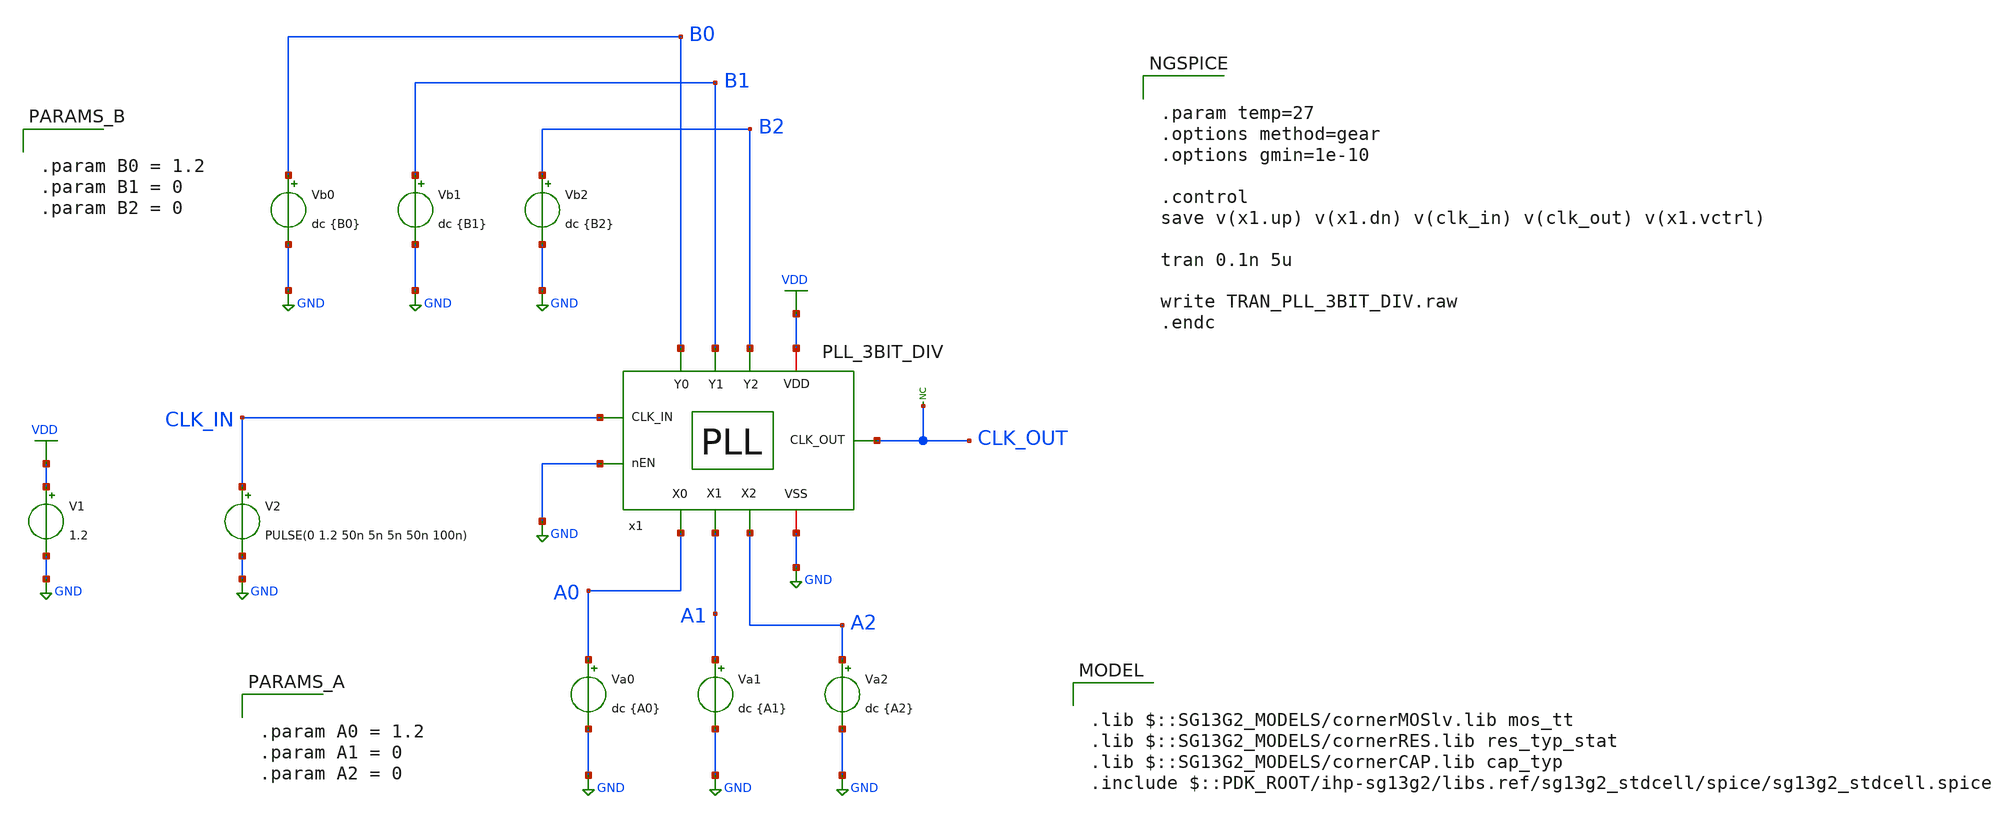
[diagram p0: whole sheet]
** sch_path: 30_MHz_Fractional_N_PLL/design_data/xschem/PLL_3BIT_DIV_TB.sch
* IHP-GmbH/IHP-Open-PDK/ihp-sg13g2/libs.tech/xschem/sg13g2_stdcells/sg13g2_or3_1.sch:
* Copyright 2023 IHP PDK Authors
* Licensed under the Apache License, Version 2.0 (the "License");

.lib $::SG13G2_MODELS/cornerMOSlv.lib mos_tt
.lib $::SG13G2_MODELS/cornerRES.lib res_typ_stat
.lib $::SG13G2_MODELS/cornerCAP.lib cap_typ
.include $::PDK_ROOT/ihp-sg13g2/libs.ref/sg13g2_stdcell/spice/sg13g2_stdcell.spice

**.subckt PLL_3BIT_DIV_TB
V1 VDD GND 1.2
V2 CLK_IN GND PULSE(0 1.2 50n 5n 5n 50n 100n)
Va0 A0 GND dc {A0}
Va1 A1 GND dc {A1}
* noconn CLK_OUT
Va2 A2 GND dc {A2}
Vb0 B0 GND dc {B0}
Vb1 B1 GND dc {B1}
Vb2 B2 GND dc {B2}
x1 CLK_IN CLK_OUT B0 B2 B1 VDD GND GND A1 A2 A0 PLL_3BIT_DIV
**** begin user architecture code


.param temp=27
.options method=gear
.options gmin=1e-10

.control
save v(x1.up) v(x1.dn) v(clk_in) v(clk_out) v(x1.vctrl)

tran 0.1n 5u

write TRAN_PLL_3BIT_DIV.raw
.endc





.param A0 = 1.2
.param A1 = 0
.param A2 = 0




.param B0 = 1.2
.param B1 = 0
.param B2 = 0




.ic V(VDD) = 1.2
.ic V(x1.up) = 0
.ic V(x1.dn) = 0
.ic V(x1.vctrl) = 0.7


**** end user architecture code
**.ends

* expanding   symbol:  PLL_3BIT_DIV.sym # of pins=11
** sym_path: 30_MHz_Fractional_N_PLL/design_data/xschem/PLL_3BIT_DIV.sym
** sch_path: 30_MHz_Fractional_N_PLL/design_data/xschem/PLL_3BIT_DIV.sch
.subckt PLL_3BIT_DIV CLK_IN CLK_OUT Y0 Y2 Y1 VDD VSS nEN X1 X2 X0
*.iopin VSS
*.iopin VDD
*.ipin CLK_IN
*.opin CLK_OUT
*.ipin X0
*.ipin X1
*.ipin nEN
*.ipin X2
*.ipin Y0
*.ipin Y1
*.ipin Y2
x3 VDD VDD VSS VSS EN BIAS_N BIAS_P nEN BIAS_GEN
x5 VDD UP VSS DN CLK_IN DIV_OUT PFD
x2 VDD BIAS_P UP VOUT_CP DN BIAS_N VSS CHRG_PUMP
x1 VOUT_CP VCTRL VSS LOOP_FILTER
x6 EN nEN VDD VSS sg13g2_inv_1
x7 X0 VCO_OUT EN DIV_OUT X1 VDD VSS X2 3BIT_FREQ_DIV
x9 Y0 VCO_OUT EN CLK_OUT Y1 VDD VSS Y2 3BIT_FREQ_DIV
x4 VDD VSS VCTRL VCO_OUT 11STG_VCO
.ends


* expanding   symbol:  BIAS_GEN.sym # of pins=8
** sym_path: 30_MHz_Fractional_N_PLL/design_data/xschem/BIAS_GEN.sym
** sch_path: 30_MHz_Fractional_N_PLL/design_data/xschem/BIAS_GEN.sch
.subckt BIAS_GEN VPWR VPB VGND VNB en bias_n bias_p enb
*.ipin en
*.opin bias_n
*.iopin VNB
*.iopin VGND
*.iopin VPB
*.iopin VPWR
*.ipin enb
*.opin bias_p
XM1 bias_p kick kick_sw VNB sg13_lv_nmos w=0.5u l=0.15u ng=1 m=1 mm_ok=1
XM2 kick_sw en VGND VNB sg13_lv_nmos w=0.5u l=0.15u ng=1 m=1 mm_ok=1
XM3 kick bias_n VGND VNB sg13_lv_nmos w=1.0u l=1.0u ng=1 m=1 mm_ok=1
XM4 bias_p bias_n net1 VNB sg13_lv_nmos w=1.0u l=1.0u ng=1 m=1 mm_ok=1
XM5 bias_n enb VGND VNB sg13_lv_nmos w=0.5u l=0.15u ng=1 m=1 mm_ok=1
XM6 bias_n bias_n VGND VNB sg13_lv_nmos w=1.0u l=1.0u ng=1 m=1 mm_ok=1
XM7 kick kick dio_mid VPB sg13_lv_pmos w=0.5u l=0.15u ng=1 m=1 mm_ok=1
XM8 bias_p bias_p VPWR VPB sg13_lv_pmos w=2.0u l=1.0u ng=1 m=1 mm_ok=1
XM9 bias_p en VPWR VPB sg13_lv_pmos w=0.5u l=0.15u ng=1 m=1 mm_ok=1
XM10 bias_n bias_p res_bot VPB sg13_lv_pmos w=4.0u l=1.0u ng=1 m=1 mm_ok=1
XM11 kick en VPWR VPB sg13_lv_pmos w=0.5u l=0.15u ng=1 m=1 mm_ok=1
XM12 dio_mid dio_mid VPWR VPB sg13_lv_pmos w=0.5u l=0.15u ng=1 m=1 mm_ok=1
XR1 VPWR res_bot sub! rhigh w=1.0e-6 l=12.0e-6 m=1 b=0 mm_ok=1
XR2 net1 VGND sub! rhigh w=1.0e-6 l=12.0e-6 m=1 b=0 mm_ok=1
.ends


* expanding   symbol:  PFD.sym # of pins=6
** sym_path: 30_MHz_Fractional_N_PLL/design_data/xschem/PFD.sym
** sch_path: 30_MHz_Fractional_N_PLL/design_data/xschem/PFD.sch
.subckt PFD vdd up vss down ref_clk vco_clk
*.iopin vdd
*.ipin ref_clk
*.iopin vss
*.ipin vco_clk
*.opin up
*.opin down
XM1 net2 vco_clk vss vss sg13_lv_nmos w=0.36u l=0.15u ng=1 m=1 mm_ok=1
XM4 net1 ref_clk net2 vss sg13_lv_nmos w=1.8u l=0.15u ng=1 m=1 mm_ok=1
XM5 net3 ref_clk net1 vss sg13_lv_nmos w=0.84u l=0.15u ng=1 m=1 mm_ok=1
XM9 net3 ref_clk ref_clk vdd sg13_lv_pmos w=0.64u l=0.15u ng=1 m=1 mm_ok=1
XM11 net7 net3 vss vss sg13_lv_nmos w=0.36u l=0.15u ng=1 m=1 mm_ok=1
XM12 vdd net3 net7 vdd sg13_lv_pmos w=0.72u l=0.15u ng=1 m=1 mm_ok=1
XM13 up net7 vss vss sg13_lv_nmos w=0.48u l=0.15u ng=1 m=1 mm_ok=1
XM14 vdd net7 up vdd sg13_lv_pmos w=0.96u l=0.15u ng=1 m=1 mm_ok=1
XM3 net1 ref_clk vdd vdd sg13_lv_pmos w=0.64u l=0.15u ng=1 m=1 mm_ok=1
XM6 net4 vco_clk vdd vdd sg13_lv_pmos w=0.64u l=0.15u ng=1 m=1 mm_ok=1
XM7 net4 vco_clk net5 vss sg13_lv_nmos w=1.8u l=0.15u ng=1 m=1 mm_ok=1
XM19 net5 ref_clk vss vss sg13_lv_nmos w=0.36u l=0.15u ng=1 m=1 mm_ok=1
XM8 net6 vco_clk net4 vss sg13_lv_nmos w=0.84u l=0.15u ng=1 m=1 mm_ok=1
XM10 net6 vco_clk vco_clk vdd sg13_lv_pmos w=0.64u l=0.15u ng=1 m=1 mm_ok=1
XM15 vdd net6 net8 vdd sg13_lv_pmos w=0.72u l=0.15u ng=1 m=1 mm_ok=1
XM16 net8 net6 vss vss sg13_lv_nmos w=0.36u l=0.15u ng=1 m=1 mm_ok=1
XM17 vdd net8 down vdd sg13_lv_pmos w=0.96u l=0.15u ng=1 m=1 mm_ok=1
XM18 down net8 vss vss sg13_lv_nmos w=0.48u l=0.15u ng=1 m=1 mm_ok=1
.ends


* expanding   symbol:  CHRG_PUMP.sym # of pins=7
** sym_path: 30_MHz_Fractional_N_PLL/design_data/xschem/CHRG_PUMP.sym
** sch_path: 30_MHz_Fractional_N_PLL/design_data/xschem/CHRG_PUMP.sch
.subckt CHRG_PUMP VP bias_p up vout down bias_n VN
*.ipin bias_p
*.ipin up
*.ipin down
*.ipin bias_n
*.iopin VN
*.iopin VP
*.opin vout
XM1 net1 bias_n VN VN sg13_lv_nmos w=1.2u l=0.13u ng=1 m=1 mm_ok=1
XM2 vout down net1 VN sg13_lv_nmos w=1.2u l=0.13u ng=1 m=1 mm_ok=1
XM3 vout net3 net2 VP sg13_lv_pmos w=0.15u l=0.13u ng=1 m=1 mm_ok=1
XM4 net2 bias_p VP VP sg13_lv_pmos w=0.15u l=0.13u ng=1 m=1 mm_ok=1
x1 VP up net3 VN INV
.ends


* expanding   symbol:  LOOP_FILTER.sym # of pins=3
** sym_path: 30_MHz_Fractional_N_PLL/design_data/xschem/LOOP_FILTER.sym
** sch_path: 30_MHz_Fractional_N_PLL/design_data/xschem/LOOP_FILTER.sch
.subckt LOOP_FILTER vin vout VN
*.iopin VN
*.ipin vin
*.opin vout
XR1 vout vin sub! rhigh w=0.6e-6 l=0.96e-6 m=1 b=0 mm_ok=1
XM1 VN net1 VN VN sg13_lv_nmos w=0.5u l=0.650u ng=1 m=15 mm_ok=1
XM2 VN vout VN VN sg13_lv_nmos w=0.15u l=0.13u ng=1 m=1 mm_ok=1
XM3 VN net1 VN VN sg13_lv_nmos w=0.5u l=0.650u ng=1 m=15 mm_ok=1
XM4 VN vout VN VN sg13_lv_nmos w=0.15u l=0.13u ng=1 m=1 mm_ok=1
XR2 net1 vin sub! rhigh w=0.5e-6 l=0.96e-6 m=1 b=0 mm_ok=1
XM5 VN vin VN VN sg13_lv_nmos w=1.5u l=0.650u ng=1 m=15 mm_ok=1
XM6 VN vin VN VN sg13_lv_nmos w=1.5u l=0.650u ng=1 m=15 mm_ok=1
.ends


* expanding   symbol:  sg13g2_stdcells/sg13g2_inv_1.sym # of pins=2
** sym_path: sg13g2_stdcells/sg13g2_inv_1.sym
** sch_path: sg13g2_stdcells/sg13g2_inv_1.sch
.subckt sg13g2_inv_1 Y A VDD VSS
*.opin Y
*.ipin A
*.iopin VDD
*.iopin VSS
XM1 Y A VSS VSS sg13_lv_nmos w=740.00n l=130.00n ng=1 m=1 mm_ok=1
XM2 Y A VDD VDD sg13_lv_pmos w=1.12u l=130.00n ng=1 m=1 mm_ok=1
.ends


* expanding   symbol:  3BIT_FREQ_DIV.sym # of pins=8
** sym_path: 30_MHz_Fractional_N_PLL/design_data/xschem/3BIT_FREQ_DIV.sym
** sch_path: 30_MHz_Fractional_N_PLL/design_data/xschem/3BIT_FREQ_DIV.sch
.subckt 3BIT_FREQ_DIV A0 CLK_IN EN CLK_OUT A1 VDD VSS A2
*.ipin CLK_IN
*.ipin EN
*.ipin A0
*.ipin A1
*.opin CLK_OUT
*.iopin VSS
*.iopin VDD
*.ipin A2
x1 VDD VSS nEQ0 net1 CLK net2 DIV_RST A0 FREQ_DIV_CELL
x2 VDD VSS nEQ1 net2 CLK net5 DIV_RST A1 FREQ_DIV_CELL
x3 net6 VDD VSS sg13g2_tiehi
x5 DIV_RST CLK_OUT net3 net3 net4 VDD VSS DFF_nCLK
x6 net7 VDD VSS sg13g2_tiehi
* noconn CLK_OUT
x7 CLK CLK_IN EN VDD VSS sg13g2_nand2_1
x4 DIV_RST nEQ2 nEQ1 nEQ0 VDD VSS sg13g2_or3_1
x8 VDD VSS nEQ2 net5 CLK Cout DIV_RST A2 FREQ_DIV_CELL
* noconn Cout
.ends


* expanding   symbol:  11STG_VCO.sym # of pins=4
** sym_path: 30_MHz_Fractional_N_PLL/design_data/xschem/11STG_VCO.sym
** sch_path: 30_MHz_Fractional_N_PLL/design_data/xschem/11STG_VCO.sch
.subckt 11STG_VCO VPWR VGND vctl Vout
*.iopin VPWR
*.iopin VGND
*.ipin vctl
*.opin Vout
XM21 mirror_pg mirror_pg VPWR VPWR sg13_lv_pmos w=0.8u l=0.13u ng=1 m=1 mm_ok=1
XM22 net1 mirror_pg VPWR VPWR sg13_lv_pmos w=0.8u l=0.13u ng=1 m=1 mm_ok=1
XM23 net2 mirror_pg VPWR VPWR sg13_lv_pmos w=0.8u l=0.13u ng=1 m=1 mm_ok=1
XM24 net3 mirror_pg VPWR VPWR sg13_lv_pmos w=0.8u l=0.13u ng=1 m=1 mm_ok=1
XM25 mirror_pg vctl VGND VGND sg13_lv_nmos w=0.6u l=0.13u ng=1 m=1 mm_ok=1
XM26 net9 vctl VGND VGND sg13_lv_nmos w=0.6u l=0.13u ng=1 m=1 mm_ok=1
XM28 net7 vctl VGND VGND sg13_lv_nmos w=0.6u l=0.13u ng=1 m=1 mm_ok=1
XM29 net13 mirror_pg VPWR VPWR sg13_lv_pmos w=0.8u l=0.13u ng=1 m=1 mm_ok=1
XM30 net12 mirror_pg VPWR VPWR sg13_lv_pmos w=0.8u l=0.13u ng=1 m=1 mm_ok=1
XM31 net10 vctl VGND VGND sg13_lv_nmos w=0.6u l=0.13u ng=1 m=1 mm_ok=1
XM32 net11 vctl VGND VGND sg13_lv_nmos w=0.6u l=0.13u ng=1 m=1 mm_ok=1
XM33 net15 mirror_pg VPWR VPWR sg13_lv_pmos w=0.8u l=0.13u ng=1 m=1 mm_ok=1
XM34 net16 mirror_pg VPWR VPWR sg13_lv_pmos w=0.8u l=0.13u ng=1 m=1 mm_ok=1
XM35 net20 vctl VGND VGND sg13_lv_nmos w=0.6u l=0.13u ng=1 m=1 mm_ok=1
XM36 net19 vctl VGND VGND sg13_lv_nmos w=0.6u l=0.13u ng=1 m=1 mm_ok=1
XM37 net24 mirror_pg VPWR VPWR sg13_lv_pmos w=0.8u l=0.13u ng=1 m=1 mm_ok=1
XM38 net23 mirror_pg VPWR VPWR sg13_lv_pmos w=0.8u l=0.13u ng=1 m=1 mm_ok=1
XM39 net21 vctl VGND VGND sg13_lv_nmos w=0.6u l=0.13u ng=1 m=1 mm_ok=1
XM40 net22 vctl VGND VGND sg13_lv_nmos w=0.6u l=0.13u ng=1 m=1 mm_ok=1
XM41 net31 mirror_pg VPWR VPWR sg13_lv_pmos w=0.8u l=0.13u ng=1 m=1 mm_ok=1
XM42 net30 mirror_pg VPWR VPWR sg13_lv_pmos w=0.8u l=0.13u ng=1 m=1 mm_ok=1
XM43 net28 vctl VGND VGND sg13_lv_nmos w=0.6u l=0.13u ng=1 m=1 mm_ok=1
XM44 net29 vctl VGND VGND sg13_lv_nmos w=0.6u l=0.13u ng=1 m=1 mm_ok=1
XM1 net8 vctl VGND VGND sg13_lv_nmos w=0.6u l=0.13u ng=1 m=1 mm_ok=1
XC12 net4 VGND cap_cmim w=6.99e-6 l=6.99e-6 m=1 mm_ok=1
XC1 net5 VGND cap_cmim w=6.99e-6 l=6.99e-6 m=1 mm_ok=1
XC2 net6 VGND cap_cmim w=6.99e-6 l=6.99e-6 m=1 mm_ok=1
XC3 net14 VGND cap_cmim w=6.99e-6 l=6.99e-6 m=1 mm_ok=1
XC4 net26 VGND cap_cmim w=6.99e-6 l=6.99e-6 m=1 mm_ok=1
XC5 net17 VGND cap_cmim w=6.99e-6 l=6.99e-6 m=1 mm_ok=1
XC6 net18 VGND cap_cmim w=6.99e-6 l=6.99e-6 m=1 mm_ok=1
XC7 net25 VGND cap_cmim w=6.99e-6 l=6.99e-6 m=1 mm_ok=1
XC8 net27 VGND cap_cmim w=6.99e-6 l=6.99e-6 m=1 mm_ok=1
XC9 net32 VGND cap_cmim w=6.99e-6 l=6.99e-6 m=1 mm_ok=1
XC10 Vout VGND cap_cmim w=6.99e-6 l=6.99e-6 m=1 mm_ok=1
x1 net1 VPWR Vout net4 VGND net9 VCO_INV
x2 net2 VPWR net4 net5 VGND net8 VCO_INV
x3 net3 VPWR net5 net6 VGND net7 VCO_INV
x4 net13 VPWR net6 net14 VGND net10 VCO_INV
x5 net12 VPWR net14 net26 VGND net11 VCO_INV
x6 net15 VPWR net26 net17 VGND net20 VCO_INV
x7 net16 VPWR net17 net18 VGND net19 VCO_INV
x8 net24 VPWR net18 net25 VGND net21 VCO_INV
x9 net23 VPWR net25 net27 VGND net22 VCO_INV
x10 net31 VPWR net27 net32 VGND net28 VCO_INV
x11 net30 VPWR net32 Vout VGND net29 VCO_INV
.ends


* expanding   symbol:  INV.sym # of pins=4
** sym_path: 30_MHz_Fractional_N_PLL/design_data/xschem/INV.sym
** sch_path: 30_MHz_Fractional_N_PLL/design_data/xschem/INV.sch
.subckt INV VP IN OUT VN
*.iopin VN
*.iopin VP
*.ipin IN
*.opin OUT
XM1 OUT IN VN VN sg13_lv_nmos w=0.15u l=0.13u ng=1 m=1 mm_ok=1
XM2 OUT IN VP VP sg13_lv_pmos w=0.3u l=0.13u ng=1 m=1 mm_ok=1
.ends


* expanding   symbol:  FREQ_DIV_CELL.sym # of pins=8
** sym_path: 30_MHz_Fractional_N_PLL/design_data/xschem/FREQ_DIV_CELL.sym
** sch_path: 30_MHz_Fractional_N_PLL/design_data/xschem/FREQ_DIV_CELL.sch
.subckt FREQ_DIV_CELL VDD VSS DIV Cin CLK Cout nRST BIT
*.ipin Cin
*.ipin CLK
*.ipin nRST
*.ipin BIT
*.opin DIV
*.opin Cout
*.iopin VSS
*.iopin VDD
x2 CLK net2 net1 net3 nRST VDD VSS DFF_nCLK
x3 DIV net2 BIT VDD VSS sg13g2_xor2_1
* noconn #net3
x1 net2 net1 Cin VDD VSS Cout HALF_ADD
.ends


* expanding   symbol:  DFF_nCLK.sym # of pins=7
** sym_path: 30_MHz_Fractional_N_PLL/design_data/xschem/DFF_nCLK.sym
** sch_path: 30_MHz_Fractional_N_PLL/design_data/xschem/DFF_nCLK.sch
.subckt DFF_nCLK nCLK Q D nQ nRST VDD VSS
*.ipin nCLK
*.ipin D
*.ipin nRST
*.opin Q
*.opin nQ
*.iopin VSS
*.iopin VDD
x1 Q nQ net1 D nRST VDD VSS sg13g2_dfrbp_1
x2 net1 nCLK VDD VSS sg13g2_inv_1
.ends


* expanding   symbol:  sg13g2_stdcells/sg13g2_nand2_1.sym # of pins=3
** sym_path: sg13g2_stdcells/sg13g2_nand2_1.sym
** sch_path: sg13g2_stdcells/sg13g2_nand2_1.sch
.subckt sg13g2_nand2_1 Y A B VDD VSS
*.iopin VDD
*.iopin VSS
*.ipin A
*.ipin B
*.opin Y
XM1 Y A net1 VSS sg13_lv_nmos w=740.00n l=130.00n ng=1 m=1 mm_ok=1
XM2 net1 B VSS VSS sg13_lv_nmos w=740.00n l=130.00n ng=1 m=1 mm_ok=1
XM3 Y A VDD VDD sg13_lv_pmos w=1.12u l=130.00n ng=1 m=1 mm_ok=1
XM4 Y B VDD VDD sg13_lv_pmos w=1.12u l=130.00n ng=1 m=1 mm_ok=1
.ends


* expanding   symbol:  sg13g2_stdcells/sg13g2_or3_1.sym # of pins=4
** sym_path: sg13g2_stdcells/sg13g2_or3_1.sym
** sch_path: sg13g2_stdcells/sg13g2_or3_1.sch
.subckt sg13g2_or3_1 X A B C VDD VSS
*.opin X
*.ipin C
*.ipin B
*.ipin A
*.iopin VDD
*.iopin VSS
XM1 net2 A VSS VSS sg13_lv_nmos w=550.00n l=130.00n ng=1 m=1 mm_ok=1
XM2 net2 B VSS VSS sg13_lv_nmos w=550.00n l=130.00n ng=1 m=1 mm_ok=1
XM3 net2 C VSS VSS sg13_lv_nmos w=550.00n l=130.00n ng=1 m=1 mm_ok=1
XM4 X net2 VSS VSS sg13_lv_nmos w=740.00n l=130.00n ng=1 m=1 mm_ok=1
XM5 net1 A VDD VDD sg13_lv_pmos w=1.000u l=130.00n ng=1 m=1 mm_ok=1
XM6 net3 B net1 VDD sg13_lv_pmos w=1.000u l=130.00n ng=1 m=1 mm_ok=1
XM7 net2 C net3 VDD sg13_lv_pmos w=1.000u l=130.00n ng=1 m=1 mm_ok=1
XM8 X net2 VDD VDD sg13_lv_pmos w=1.12u l=130.00n ng=1 m=1 mm_ok=1
.ends


* expanding   symbol:  VCO_INV.sym # of pins=6
** sym_path: 30_MHz_Fractional_N_PLL/design_data/xschem/VCO_INV.sym
** sch_path: 30_MHz_Fractional_N_PLL/design_data/xschem/VCO_INV.sch
.subckt VCO_INV VPWR VPB A Y VNB VGND
*.iopin VPWR
*.iopin VGND
*.ipin A
*.opin Y
*.iopin VPB
*.iopin VNB
XM2 Y A VPWR VPB sg13_lv_pmos w=2u l=0.13u ng=1 m=1 mm_ok=1
XM1 Y A VGND VNB sg13_lv_nmos w=1u l=0.13u ng=1 m=1 mm_ok=1
.ends


* expanding   symbol:  sg13g2_stdcells/sg13g2_xor2_1.sym # of pins=3
** sym_path: sg13g2_stdcells/sg13g2_xor2_1.sym
** sch_path: sg13g2_stdcells/sg13g2_xor2_1.sch
.subckt sg13g2_xor2_1 X A B VDD VSS
*.opin X
*.ipin B
*.ipin A
*.iopin VDD
*.iopin VSS
XM1 net1 A VSS VSS sg13_lv_nmos w=550.00n l=130.00n ng=1 m=1 mm_ok=1
XM2 net1 B VSS VSS sg13_lv_nmos w=550.00n l=130.00n ng=1 m=1 mm_ok=1
XM3 X net1 VSS VSS sg13_lv_nmos w=740.00n l=130.00n ng=1 m=1 mm_ok=1
XM4 X B net3 VSS sg13_lv_nmos w=740.00n l=130.00n ng=1 m=1 mm_ok=1
XM5 net3 A VSS VSS sg13_lv_nmos w=740.00n l=130.00n ng=1 m=1 mm_ok=1
XM6 net4 A VDD VDD sg13_lv_pmos w=1.000u l=130.00n ng=1 m=1 mm_ok=1
XM7 net1 B net4 VDD sg13_lv_pmos w=1.000u l=130.00n ng=1 m=1 mm_ok=1
XM8 net2 A VDD VDD sg13_lv_pmos w=1.12u l=130.00n ng=1 m=1 mm_ok=1
XM9 X net1 net2 VDD sg13_lv_pmos w=1.12u l=130.00n ng=1 m=1 mm_ok=1
XM10 net2 B VDD VDD sg13_lv_pmos w=1.12u l=130.00n ng=1 m=1 mm_ok=1
.ends


* expanding   symbol:  HALF_ADD.sym # of pins=6
** sym_path: 30_MHz_Fractional_N_PLL/design_data/xschem/HALF_ADD.sym
** sch_path: 30_MHz_Fractional_N_PLL/design_data/xschem/HALF_ADD.sch
.subckt HALF_ADD inB sum inA VDD VSS cout
*.ipin inA
*.ipin inB
*.opin sum
*.opin cout
*.iopin VSS
*.iopin VDD
x1 sum inA inB VDD VSS sg13g2_xor2_1
x2 cout inA inB VDD VSS sg13g2_and2_1
.ends


* expanding   symbol:  sg13g2_stdcells/sg13g2_dfrbp_1.sym # of pins=5
** sym_path: sg13g2_stdcells/sg13g2_dfrbp_1.sym
** sch_path: sg13g2_stdcells/sg13g2_dfrbp_1.sch
.subckt sg13g2_dfrbp_1 Q Q_N CLK D RESET_B VDD VSS
*.ipin D
*.ipin RESET_B
*.ipin CLK
*.opin Q
*.opin Q_N
*.iopin VDD
*.iopin VSS
XM1 Db D net10 VSS sg13_lv_nmos w=420.00n l=130.00n ng=1 m=1 mm_ok=1
XM2 net10 RESET_B VSS VSS sg13_lv_nmos w=420.00n l=130.00n ng=1 m=1 mm_ok=1
XM3 net1 clkneg net9 VSS sg13_lv_nmos w=420.00n l=130.00n ng=1 m=1 mm_ok=1
XM4 net9 net1 VSS VSS sg13_lv_nmos w=420.00n l=130.00n ng=1 m=1 mm_ok=1
XM5 net1 net1 net5 VSS sg13_lv_nmos w=420.00n l=130.00n ng=1 m=1 mm_ok=1
XM6 net5 RESET_B VSS VSS sg13_lv_nmos w=420.00n l=130.00n ng=1 m=1 mm_ok=1
XM7 Q_N net1 VSS VSS sg13_lv_nmos w=740.00n l=130.00n ng=1 m=1 mm_ok=1
XM8 net2 net1 VSS VSS sg13_lv_nmos w=740.00n l=130.00n ng=1 m=1 mm_ok=1
XM9 Q net2 VSS VSS sg13_lv_nmos w=740.00n l=130.00n ng=1 m=1 mm_ok=1
XM10 clkneg CLK VSS VSS sg13_lv_nmos w=740.00n l=130.00n ng=1 m=1 mm_ok=1
XM11 clkpos clkneg VSS VSS sg13_lv_nmos w=740.00n l=130.00n ng=1 m=1 mm_ok=1
XM12 Db clkneg net3 VSS sg13_lv_nmos w=420.00n l=130.00n ng=1 m=1 mm_ok=1
XM13 net3 clkpos net8 VSS sg13_lv_nmos w=420.00n l=130.00n ng=1 m=1 mm_ok=1
XM14 net8 net3 net4 VSS sg13_lv_nmos w=420.00n l=130.00n ng=1 m=1 mm_ok=1
XM15 net4 RESET_B VSS VSS sg13_lv_nmos w=420.00n l=130.00n ng=1 m=1 mm_ok=1
XM16 net3 net3 VSS VSS sg13_lv_nmos w=740.00n l=130.00n ng=1 m=1 mm_ok=1
XM17 net3 clkpos net1 VSS sg13_lv_nmos w=740.00n l=130.00n ng=1 m=1 mm_ok=1
XM18 Db RESET_B VDD VDD sg13_lv_pmos w=420.00n l=130.00n ng=1 m=1 mm_ok=1
XM19 Db D VDD VDD sg13_lv_pmos w=420.00n l=130.00n ng=1 m=1 mm_ok=1
XM20 net7 net1 VDD VDD sg13_lv_pmos w=420.00n l=130.00n ng=1 m=1 mm_ok=1
XM21 net1 clkpos net7 VDD sg13_lv_pmos w=420.00n l=130.00n ng=1 m=1 mm_ok=1
XM22 net1 net1 VDD VDD sg13_lv_pmos w=420.00n l=130.00n ng=1 m=1 mm_ok=1
XM23 net1 RESET_B VDD VDD sg13_lv_pmos w=420.00n l=130.00n ng=1 m=1 mm_ok=1
XM24 Q_N net1 VDD VDD sg13_lv_pmos w=1.12u l=130.00n ng=1 m=1 mm_ok=1
XM25 net2 net1 VDD VDD sg13_lv_pmos w=1.12u l=130.00n ng=1 m=1 mm_ok=1
XM26 Q net2 VDD VDD sg13_lv_pmos w=1.12u l=130.00n ng=1 m=1 mm_ok=1
XM27 clkneg CLK VDD VDD sg13_lv_pmos w=1.12u l=130.00n ng=1 m=1 mm_ok=1
XM28 clkpos clkneg VDD VDD sg13_lv_pmos w=1.12u l=130.00n ng=1 m=1 mm_ok=1
XM29 Db clkpos net3 VDD sg13_lv_pmos w=420.00n l=130.00n ng=1 m=1 mm_ok=1
XM30 net6 net3 VDD VDD sg13_lv_pmos w=420.00n l=130.00n ng=1 m=1 mm_ok=1
XM31 net3 clkneg net6 VDD sg13_lv_pmos w=420.00n l=130.00n ng=1 m=1 mm_ok=1
XM32 net3 RESET_B VDD VDD sg13_lv_pmos w=420.00n l=130.00n ng=1 m=1 mm_ok=1
XM33 net3 net3 VDD VDD sg13_lv_pmos w=1.000u l=130.00n ng=1 m=1 mm_ok=1
XM34 net3 clkneg net1 VDD sg13_lv_pmos w=1.000u l=130.00n ng=1 m=1 mm_ok=1
.ends


* expanding   symbol:  sg13g2_stdcells/sg13g2_and2_1.sym # of pins=3
** sym_path: sg13g2_stdcells/sg13g2_and2_1.sym
** sch_path: sg13g2_stdcells/sg13g2_and2_1.sch
.subckt sg13g2_and2_1 X A B VDD VSS
*.ipin A
*.ipin B
*.opin X
*.iopin VDD
*.iopin VSS
XM1 net1 A net2 VSS sg13_lv_nmos w=640.00n l=130.00n ng=1 m=1 mm_ok=1
XM2 net2 B VSS VSS sg13_lv_nmos w=640.00n l=130.00n ng=1 m=1 mm_ok=1
XM3 X net1 VSS VSS sg13_lv_nmos w=740.00n l=130.00n ng=1 m=1 mm_ok=1
XM4 net1 B VDD VDD sg13_lv_pmos w=840.00n l=130.00n ng=1 m=1 mm_ok=1
XM5 net1 A VDD VDD sg13_lv_pmos w=840.00n l=130.00n ng=1 m=1 mm_ok=1
XM6 X net1 VDD VDD sg13_lv_pmos w=1.12u l=130.00n ng=1 m=1 mm_ok=1
.ends

.GLOBAL GND
.GLOBAL VDD
.end
